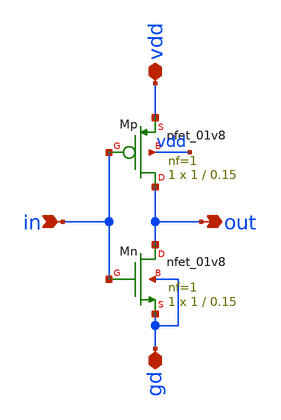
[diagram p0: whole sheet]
** sch_path: analog/klayout/production/final_merge_20260923/testbenches/cace/analog/xschem/demo_inv.sch
**.subckt demo_inv in vdd gd out
*.ipin in
*.iopin vdd
*.iopin gd
*.opin out
XMn out in gd gd sky130_fd_pr__nfet_01v8 L=0.15 W=1 nf=1 ad='int((1 + 1)/2) * 1 / 1 * 0.29' as='int((1 + 2)/2) * 1 / 1 * 0.29'
+ pd='2*int((1 + 1)/2) * (1 / 1 + 0.29)' ps='2*int((1 + 2)/2) * (1 / 1 + 0.29)' nrd='0.29 / 1 ' nrs='0.29 / 1 '
+ sa=0 sb=0 sd=0 mult=1 m=1
XMp out in vdd vdd sky130_fd_pr__pfet_01v8 L=0.15 W=1 nf=1 ad='int((1 + 1)/2) * 1 / 1 * 0.29' as='int((1 + 2)/2) * 1 / 1 * 0.29'
+ pd='2*int((1 + 1)/2) * (1 / 1 + 0.29)' ps='2*int((1 + 2)/2) * (1 / 1 + 0.29)' nrd='0.29 / 1 ' nrs='0.29 / 1 '
+ sa=0 sb=0 sd=0 mult=1 m=1
**.ends
.end
